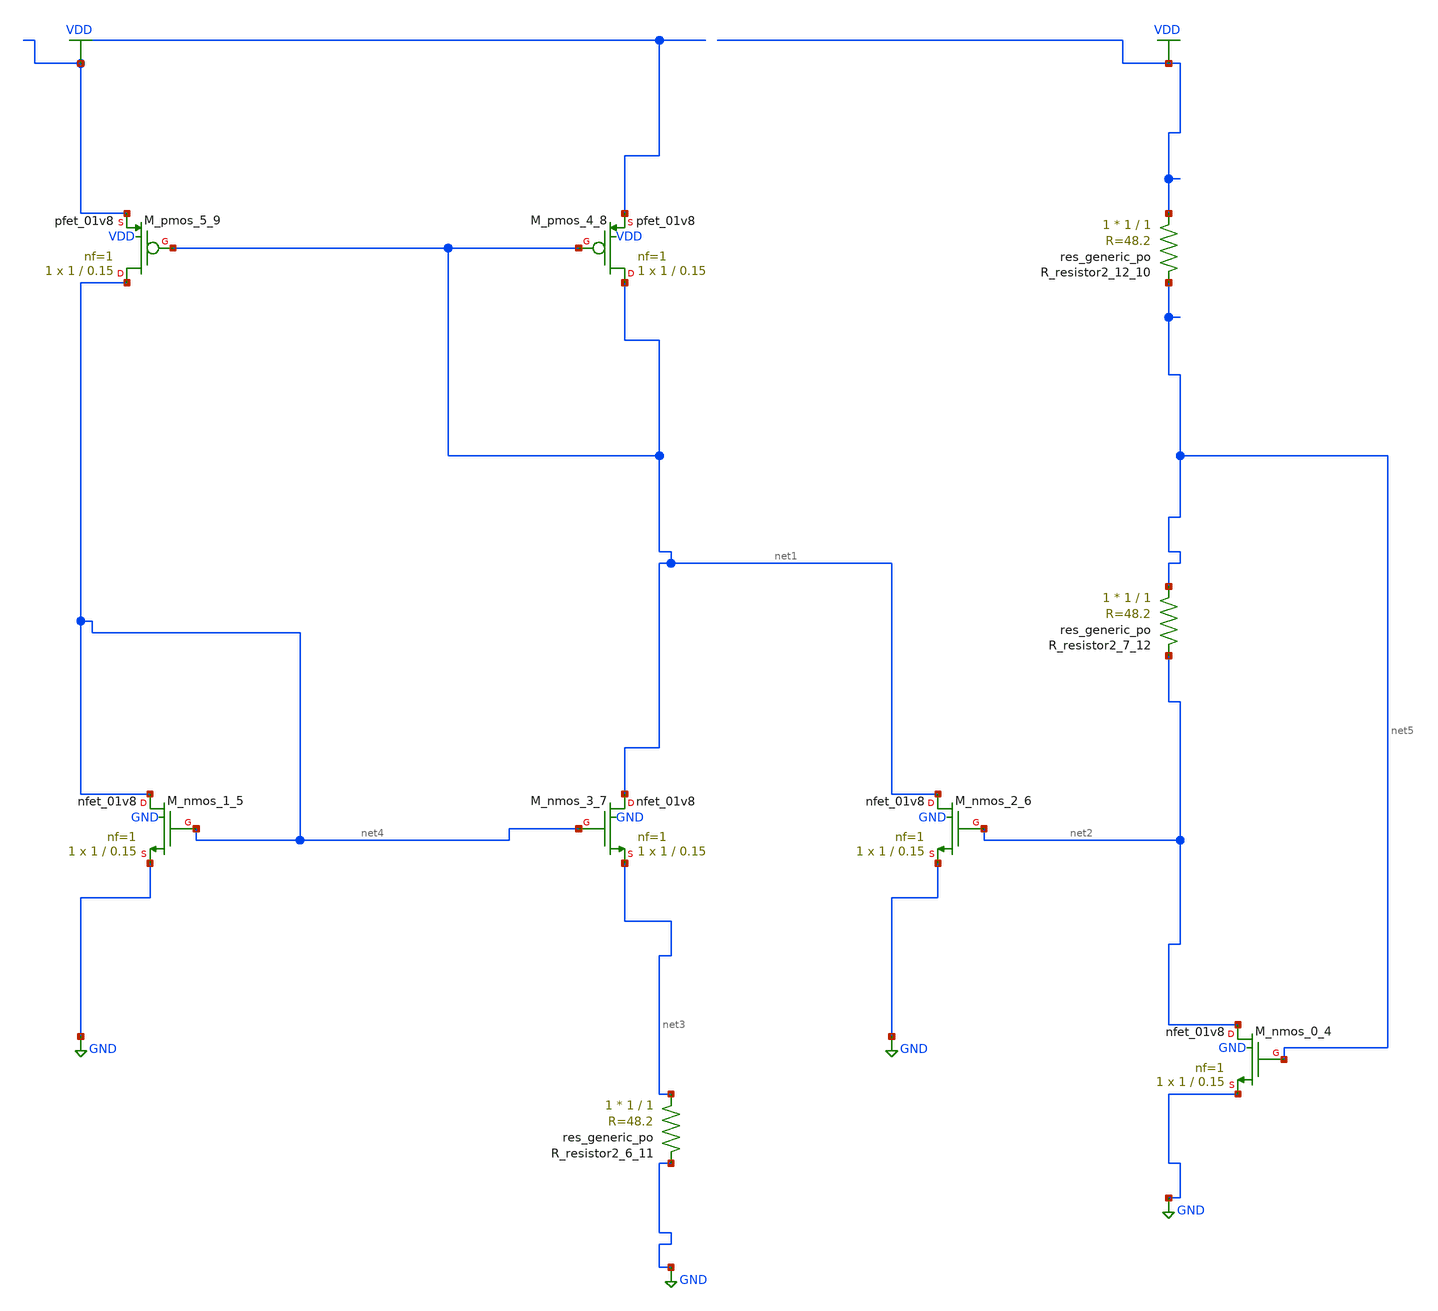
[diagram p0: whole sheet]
** sch_path: schematics/AMSNet/769.sch
**.subckt 769
XM_nmos_0_4 net2 net5 GND GND sky130_fd_pr__nfet_01v8 L=0.15 W=1 nf=1 ad='int((1 + 1)/2) * 1 / 1 * 0.29'
+ as='int((1 + 2)/2) * 1 / 1 * 0.29' pd='2*int((1 + 1)/2) * (1 / 1 + 0.29)' ps='2*int((1 + 2)/2) * (1 / 1 + 0.29)'
+ nrd='0.29 / 1 ' nrs='0.29 / 1 ' sa=0 sb=0 sd=0 mult=1 m=1
XM_nmos_1_5 net4 net4 GND GND sky130_fd_pr__nfet_01v8 L=0.15 W=1 nf=1 ad='int((1 + 1)/2) * 1 / 1 * 0.29'
+ as='int((1 + 2)/2) * 1 / 1 * 0.29' pd='2*int((1 + 1)/2) * (1 / 1 + 0.29)' ps='2*int((1 + 2)/2) * (1 / 1 + 0.29)'
+ nrd='0.29 / 1 ' nrs='0.29 / 1 ' sa=0 sb=0 sd=0 mult=1 m=1
XM_nmos_2_6 net1 net2 GND GND sky130_fd_pr__nfet_01v8 L=0.15 W=1 nf=1 ad='int((1 + 1)/2) * 1 / 1 * 0.29'
+ as='int((1 + 2)/2) * 1 / 1 * 0.29' pd='2*int((1 + 1)/2) * (1 / 1 + 0.29)' ps='2*int((1 + 2)/2) * (1 / 1 + 0.29)'
+ nrd='0.29 / 1 ' nrs='0.29 / 1 ' sa=0 sb=0 sd=0 mult=1 m=1
XM_nmos_3_7 net1 net4 net3 GND sky130_fd_pr__nfet_01v8 L=0.15 W=1 nf=1 ad='int((1 + 1)/2) * 1 / 1 * 0.29'
+ as='int((1 + 2)/2) * 1 / 1 * 0.29' pd='2*int((1 + 1)/2) * (1 / 1 + 0.29)' ps='2*int((1 + 2)/2) * (1 / 1 + 0.29)'
+ nrd='0.29 / 1 ' nrs='0.29 / 1 ' sa=0 sb=0 sd=0 mult=1 m=1
XM_pmos_4_8 net1 net1 VDD VDD sky130_fd_pr__pfet_01v8 L=0.15 W=1 nf=1 ad='int((1 + 1)/2) * 1 / 1 * 0.29'
+ as='int((1 + 2)/2) * 1 / 1 * 0.29' pd='2*int((1 + 1)/2) * (1 / 1 + 0.29)' ps='2*int((1 + 2)/2) * (1 / 1 + 0.29)'
+ nrd='0.29 / 1 ' nrs='0.29 / 1 ' sa=0 sb=0 sd=0 mult=1 m=1
XM_pmos_5_9 net4 net1 VDD VDD sky130_fd_pr__pfet_01v8 L=0.15 W=1 nf=1 ad='int((1 + 1)/2) * 1 / 1 * 0.29'
+ as='int((1 + 2)/2) * 1 / 1 * 0.29' pd='2*int((1 + 1)/2) * (1 / 1 + 0.29)' ps='2*int((1 + 2)/2) * (1 / 1 + 0.29)'
+ nrd='0.29 / 1 ' nrs='0.29 / 1 ' sa=0 sb=0 sd=0 mult=1 m=1
XR_resistor2_12_10 VDD net5 sky130_fd_pr__res_generic_po W=1 L=1 m=1
XR_resistor2_6_11 net3 GND sky130_fd_pr__res_generic_po W=1 L=1 m=1
XR_resistor2_7_12 net5 net2 sky130_fd_pr__res_generic_po W=1 L=1 m=1
**.ends
.GLOBAL GND
.GLOBAL VDD
.end
